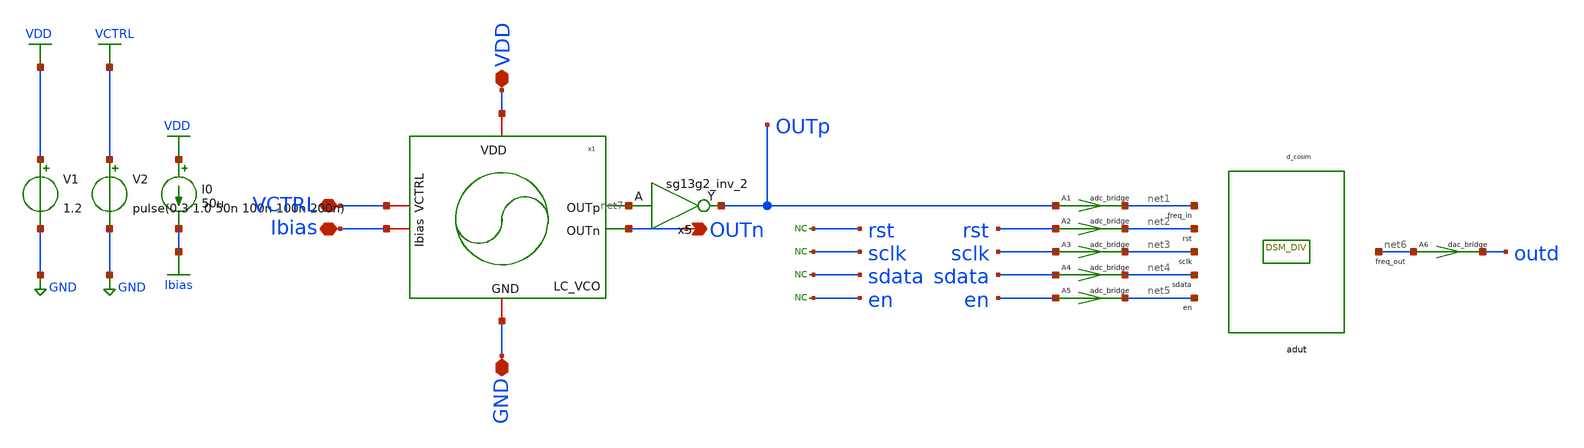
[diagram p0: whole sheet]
** sch_path: schematic/blocks/top-pll/LCVCO_DSM_tb.sch
* IHP-GmbH/IHP-Open-PDK/ihp-sg13g2/libs.tech/xschem/sg13g2_stdcells/sg13g2_inv_2.sch:
* Copyright 2023 IHP PDK Authors
* Licensed under the Apache License, Version 2.0 (the "License");
**.subckt LCVCO_DSM_tb OUTn VDD VCTRL GND Ibias
*.opin OUTn
*.iopin VDD
*.iopin VCTRL
*.iopin GND
*.iopin Ibias
V1 VDD GND 1.2
V2 VCTRL GND pulse(0.3 1.0 50n 100n 100n 200n)
I0 VDD Ibias 50u
x5 OUTp net7 VDD GND sg13g2_inv_2
x1 VDD net7 OUTn Ibias VCTRL GND LC_VCO
adut [ net1 net2 net3 net4 net5 ] [ net6 ] null dut
.model dut d_cosim simulation=./../dsm_and_freq_divider.so
A1 [ OUTp ] [ net1 ] adc1
.model adc1 adc_bridge in_low=0.4 in_high=0.6
A2 [ rst ] [ net2 ] adc1
.model adc1 adc_bridge in_low=0.4 in_high=0.6
A3 [ sclk ] [ net3 ] adc1
.model adc1 adc_bridge in_low=0.4 in_high=0.6
A4 [ sdata ] [ net4 ] adc1
.model adc1 adc_bridge in_low=0.4 in_high=0.6
A5 [ en ] [ net5 ] adc1
.model adc1 adc_bridge in_low=0.4 in_high=0.6
A6 [ net6 ] [ outd ] dac1
.model dac1 dac_bridge out_low=0 out_high=1.2
* noconn rst
* noconn sclk
* noconn sdata
* noconn en
**** begin user architecture code



.lib cornerMOSlv.lib mos_tt
.lib cornerMOShv.lib mos_tt
.lib cornerHBT.lib hbt_typ
.lib cornerRES.lib res_typ
.lib cornerCAP.lib cap_typ_stat
.include /foss/pdks/ihp-sg13g2/libs.ref/sg13g2_stdcell/spice/sg13g2_stdcell.spice
.global VDD GND







.include ./IHP_4nH_Inductor.spice
.param temp=27
.save v(OUTp) v(Vctrl)
.save v(dout) v(sdata) v(sclk) v(en) v(rst)
.save v(dsm_clk) v(outd)
.control
.options maxstep=50p reltol=1e-3 abstol=1e-6

*.ic v(OUTp)=0.6
tran 0.5n 1m
remzerovec
linearize v(OUTp) v(Vctrl) v(outd)

    let n_pts = length(time)
    let freq_vector = unitvec(n_pts) * 0

    * Advanced script to calculate instantaneous frequency
    let i = 1
    let last_cross = 0
    while i < length(time)
        if (v(OUTp)[i] >= 0.6) & (v(OUTp)[i-1] < 0.6)
            let current_cross = time[i]
            let period = current_cross - last_cross
            let inst_freq = 1 / period
            let freq_vector[i] = inst_freq
            let last_cross = current_cross
        else
            let freq_vector[i] = freq_vector[i-1]
        end
        let i = i + 1
    end

* Save transient waveform to raw file
write LCVCO_DSM.raw

*quit 0
.endc


* to generate following file copy stimuli.test
* to the simulation directory and run simulation -> Utile Stimuli Editor (GUI),
* and press 'Translate'
.include stimuli_test.cir



**** end user architecture code
**.ends

* expanding   symbol:  sg13g2_stdcells/sg13g2_inv_2.sym # of pins=2
** sym_path: sg13g2_stdcells/sg13g2_inv_2.sym
** sch_path: sg13g2_stdcells/sg13g2_inv_2.sch
.subckt sg13g2_inv_2 Y A VDD VSS
*.opin Y
*.ipin A
*.iopin VDD
*.iopin VSS
XM1 Y A VSS VSS sg13_lv_nmos w=1.48u l=130.00n ng=2 m=1 mm_ok=1
XM2 Y A VDD VDD sg13_lv_pmos w=2.24u l=130.00n ng=2 m=1 mm_ok=1
.ends


* expanding   symbol:
*+  /foss/designs/iic_osic_tools/frac-n-pll-vco-unic_cass/schematic/blocks/lc-vco/LC_VCO.sym # of pins=6
** sym_path: /foss/designs/iic_osic_tools/frac-n-pll-vco-unic_cass/schematic/blocks/lc-vco/LC_VCO.sym
** sch_path: /foss/designs/iic_osic_tools/frac-n-pll-vco-unic_cass/schematic/blocks/lc-vco/LC_VCO.sch
.subckt LC_VCO VDD OUTp OUTn Ibias VCTRL GND
*.iopin VDD
*.opin OUTp
*.opin OUTn
*.iopin GND
*.iopin VCTRL
*.iopin Ibias
XM6 net1 Ibias GND GND sg13_lv_nmos w=1u l=0.15u ng=1 m=60 mm_ok=1
XM5 Ibias Ibias GND GND sg13_lv_nmos w=1u l=0.15u ng=1 m=1 mm_ok=1
XM4 OUTp OUTn VDD VDD sg13_lv_pmos w=8.5u l=0.5u ng=1 m=13 mm_ok=1
X5M3 OUTn OUTp VDD VDD sg13_lv_pmos w=8.5u l=0.5u ng=1 m=13 mm_ok=1
XM2 OUTp OUTn net1 GND sg13_lv_nmos w=2u l=0.5u ng=1 m=12 mm_ok=1
XM1 OUTn OUTp net1 GND sg13_lv_nmos w=2u l=0.5u ng=1 m=12 mm_ok=1
XC3 OUTp OUTn cap_cmim w=4.0e-6 l=4.0e-6 m=13.6 mm_ok=1
XMv2 OUTp VCTRL OUTp VDD sg13_lv_pmos w=4u l=4u ng=1 m=22 mm_ok=1
XMv1 OUTn VCTRL OUTn VDD sg13_lv_pmos w=4u l=4u ng=1 m=22 mm_ok=1
XR1 OUTp OUTn sub! rhigh w=1e-6 l=1e-6 m=1.23 b=0 mm_ok=1
x1 OUTn OUTp ihp_4nh_inductor
.ends

.GLOBAL GND
.GLOBAL VDD
.GLOBAL VCTRL
.GLOBAL Ibias
.end
